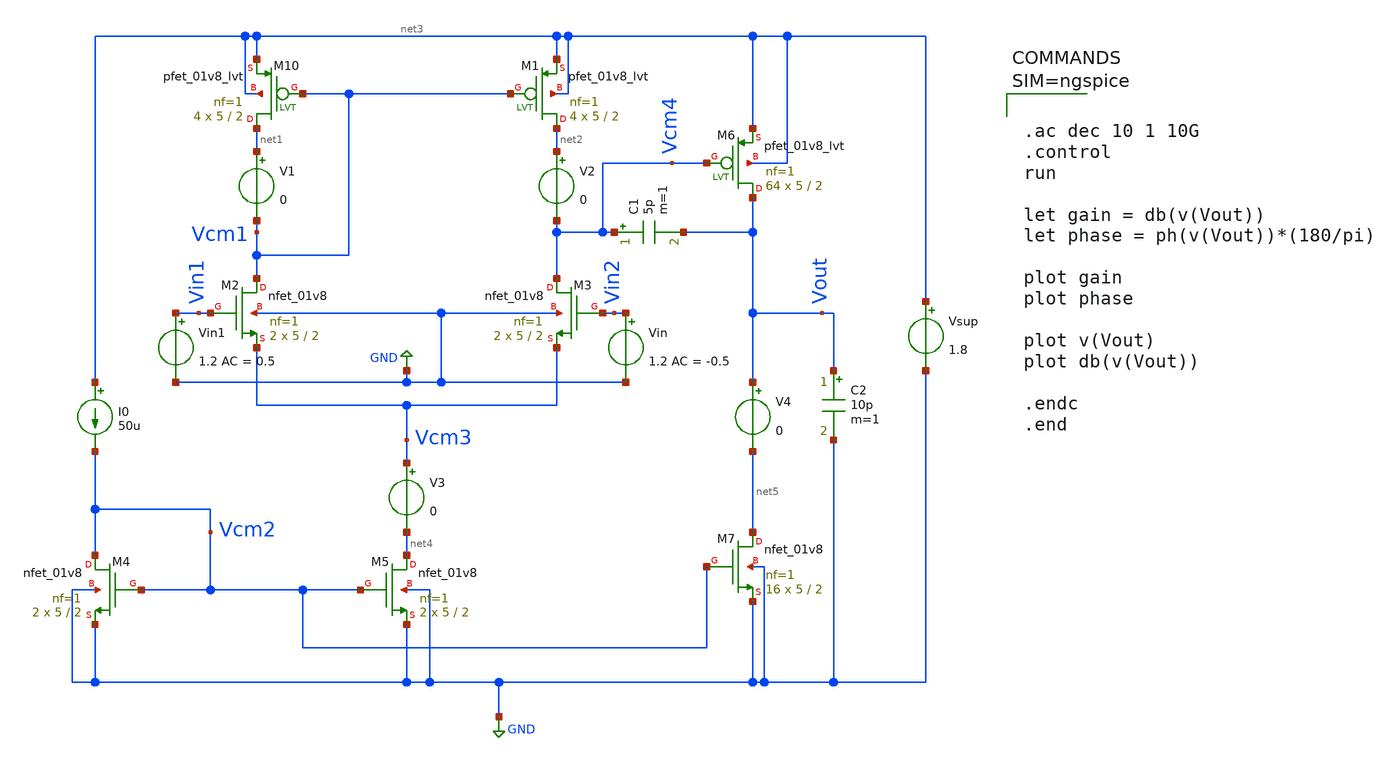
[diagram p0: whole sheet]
** sch_path: sch/OP-AMP_2stage.sch
**.subckt OP-AMP_2stage
XM10 net1 Vcm1 net3 net3 sky130_fd_pr__pfet_01v8_lvt L=2 W=5 nf=1 ad='int((1 + 1)/2) * 5 / 1 * 0.29'
+ as='int((1 + 2)/2) * 5 / 1 * 0.29' pd='2*int((1 + 1)/2) * (5 / 1 + 0.29)' ps='2*int((1 + 2)/2) * (5 / 1 + 0.29)'
+ nrd='0.29 / 5 ' nrs='0.29 / 5 ' sa=0 sb=0 sd=0 mult=4 m=4
XM2 Vcm1 Vin1 Vcm3 GND sky130_fd_pr__nfet_01v8 L=2 W=5 nf=1 ad='int((1 + 1)/2) * 5 / 1 * 0.29' as='int((1 + 2)/2) * 5 / 1 * 0.29'
+ pd='2*int((1 + 1)/2) * (5 / 1 + 0.29)' ps='2*int((1 + 2)/2) * (5 / 1 + 0.29)' nrd='0.29 / 5 ' nrs='0.29 / 5 '
+ sa=0 sb=0 sd=0 mult=2 m=2
XM1 net2 Vcm1 net3 net3 sky130_fd_pr__pfet_01v8_lvt L=2 W=5 nf=1 ad='int((1 + 1)/2) * 5 / 1 * 0.29' as='int((1 + 2)/2) * 5 / 1 * 0.29'
+ pd='2*int((1 + 1)/2) * (5 / 1 + 0.29)' ps='2*int((1 + 2)/2) * (5 / 1 + 0.29)' nrd='0.29 / 5 ' nrs='0.29 / 5 '
+ sa=0 sb=0 sd=0 mult=4 m=4
V1 net1 Vcm1 0
V2 net2 Vcm4 0
XM3 Vcm4 Vin2 Vcm3 GND sky130_fd_pr__nfet_01v8 L=2 W=5 nf=1 ad='int((1 + 1)/2) * 5 / 1 * 0.29' as='int((1 + 2)/2) * 5 / 1 * 0.29'
+ pd='2*int((1 + 1)/2) * (5 / 1 + 0.29)' ps='2*int((1 + 2)/2) * (5 / 1 + 0.29)' nrd='0.29 / 5 ' nrs='0.29 / 5 '
+ sa=0 sb=0 sd=0 mult=2 m=2
V3 Vcm3 net4 0
Vin Vin2 GND 1.2 AC = -0.5
XM4 Vcm2 Vcm2 GND GND sky130_fd_pr__nfet_01v8 L=2 W=5 nf=1 ad='int((1 + 1)/2) * 5 / 1 * 0.29' as='int((1 + 2)/2) * 5 / 1 * 0.29'
+ pd='2*int((1 + 1)/2) * (5 / 1 + 0.29)' ps='2*int((1 + 2)/2) * (5 / 1 + 0.29)' nrd='0.29 / 5 ' nrs='0.29 / 5 '
+ sa=0 sb=0 sd=0 mult=2 m=2
XM5 net4 Vcm2 GND GND sky130_fd_pr__nfet_01v8 L=2 W=5 nf=1 ad='int((1 + 1)/2) * 5 / 1 * 0.29' as='int((1 + 2)/2) * 5 / 1 * 0.29'
+ pd='2*int((1 + 1)/2) * (5 / 1 + 0.29)' ps='2*int((1 + 2)/2) * (5 / 1 + 0.29)' nrd='0.29 / 5 ' nrs='0.29 / 5 '
+ sa=0 sb=0 sd=0 mult=2 m=2
I0 net3 Vcm2 50u
Vsup net3 GND 1.8
XM6 Vout Vcm4 net3 net3 sky130_fd_pr__pfet_01v8_lvt L=2 W=5 nf=1 ad='int((1 + 1)/2) * 5 / 1 * 0.29' as='int((1 + 2)/2) * 5 / 1 * 0.29'
+ pd='2*int((1 + 1)/2) * (5 / 1 + 0.29)' ps='2*int((1 + 2)/2) * (5 / 1 + 0.29)' nrd='0.29 / 5 ' nrs='0.29 / 5 '
+ sa=0 sb=0 sd=0 mult=64 m=64
XM7 net5 Vcm2 GND GND sky130_fd_pr__nfet_01v8 L=2 W=5 nf=1 ad='int((1 + 1)/2) * 5 / 1 * 0.29' as='int((1 + 2)/2) * 5 / 1 * 0.29'
+ pd='2*int((1 + 1)/2) * (5 / 1 + 0.29)' ps='2*int((1 + 2)/2) * (5 / 1 + 0.29)' nrd='0.29 / 5 ' nrs='0.29 / 5 '
+ sa=0 sb=0 sd=0 mult=16 m=16
C1 Vcm4 Vout 5p m=1
C2 Vout GND 10p m=1
V4 Vout net5 0
Vin1 Vin1 GND 1.2 AC = 0.5
**** begin user architecture code

** opencircuitdesign pdks install
.lib $::SKYWATER_MODELS/sky130.lib.spice tt




.ac dec 10 1 10G
.control
run

let gain = db(v(Vout))
let phase = ph(v(Vout))*(180/pi)

plot gain
plot phase

plot v(Vout)
plot db(v(Vout))

.endc
.end



**** end user architecture code
**.ends
.GLOBAL GND
.end
